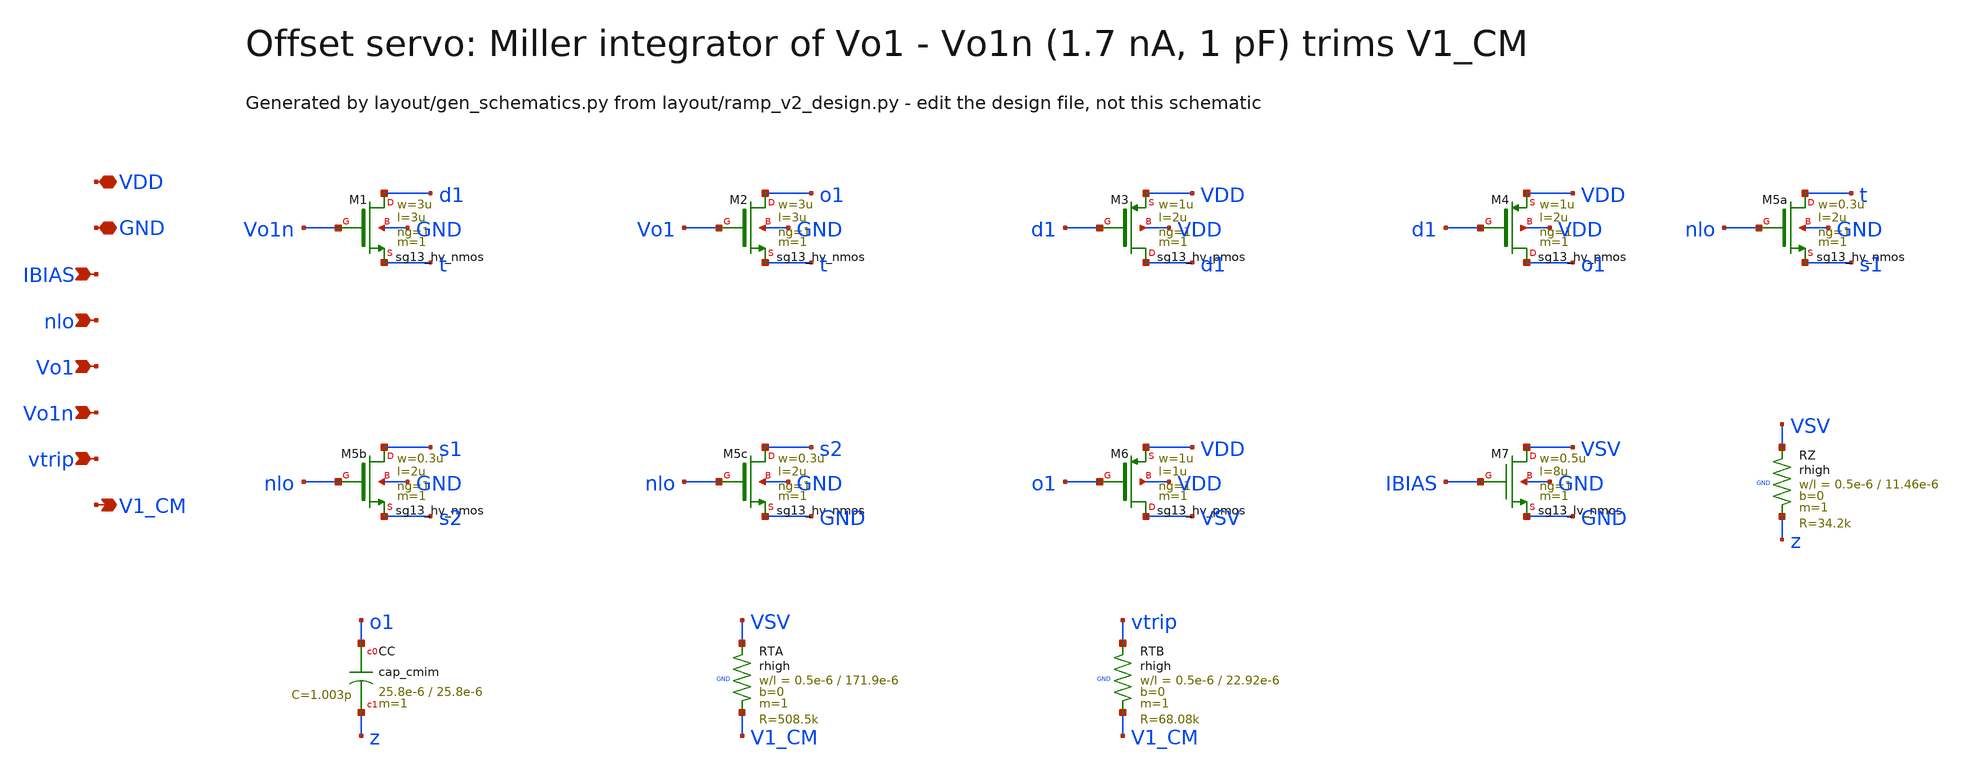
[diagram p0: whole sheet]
** sch_path: Design Files/RAMP/RAMP-V2/SERVO_V2.sch
**.subckt SERVO_V2 VDD GND IBIAS nlo Vo1 Vo1n vtrip V1_CM
*.iopin VDD
*.iopin GND
*.ipin IBIAS
*.ipin nlo
*.ipin Vo1
*.ipin Vo1n
*.ipin vtrip
*.opin V1_CM
XM1 d1 Vo1n t GND sg13_hv_nmos w=3u l=3u ng=1 m=1 mm_ok=1
XM2 o1 Vo1 t GND sg13_hv_nmos w=3u l=3u ng=1 m=1 mm_ok=1
XM3 d1 d1 VDD VDD sg13_hv_pmos w=1u l=2u ng=1 m=1 mm_ok=1
XM4 o1 d1 VDD VDD sg13_hv_pmos w=1u l=2u ng=1 m=1 mm_ok=1
XM5a t nlo s1 GND sg13_hv_nmos w=0.3u l=2u ng=1 m=1 mm_ok=1
XM5b s1 nlo s2 GND sg13_hv_nmos w=0.3u l=2u ng=1 m=1 mm_ok=1
XM5c s2 nlo GND GND sg13_hv_nmos w=0.3u l=2u ng=1 m=1 mm_ok=1
XM6 VSV o1 VDD VDD sg13_hv_pmos w=1u l=1u ng=1 m=1 mm_ok=1
XM7 VSV IBIAS GND GND sg13_lv_nmos w=0.5u l=8u ng=1 m=1 mm_ok=1
XRZ VSV z GND rhigh w=0.5e-6 l=11.46e-6 m=1 b=0 mm_ok=1
XCC o1 z cap_cmim w=25.8e-6 l=25.8e-6 m=1 mm_ok=1
XRTA VSV V1_CM GND rhigh w=0.5e-6 l=171.9e-6 m=1 b=0 mm_ok=1
XRTB vtrip V1_CM GND rhigh w=0.5e-6 l=22.92e-6 m=1 b=0 mm_ok=1
**.ends
.end
